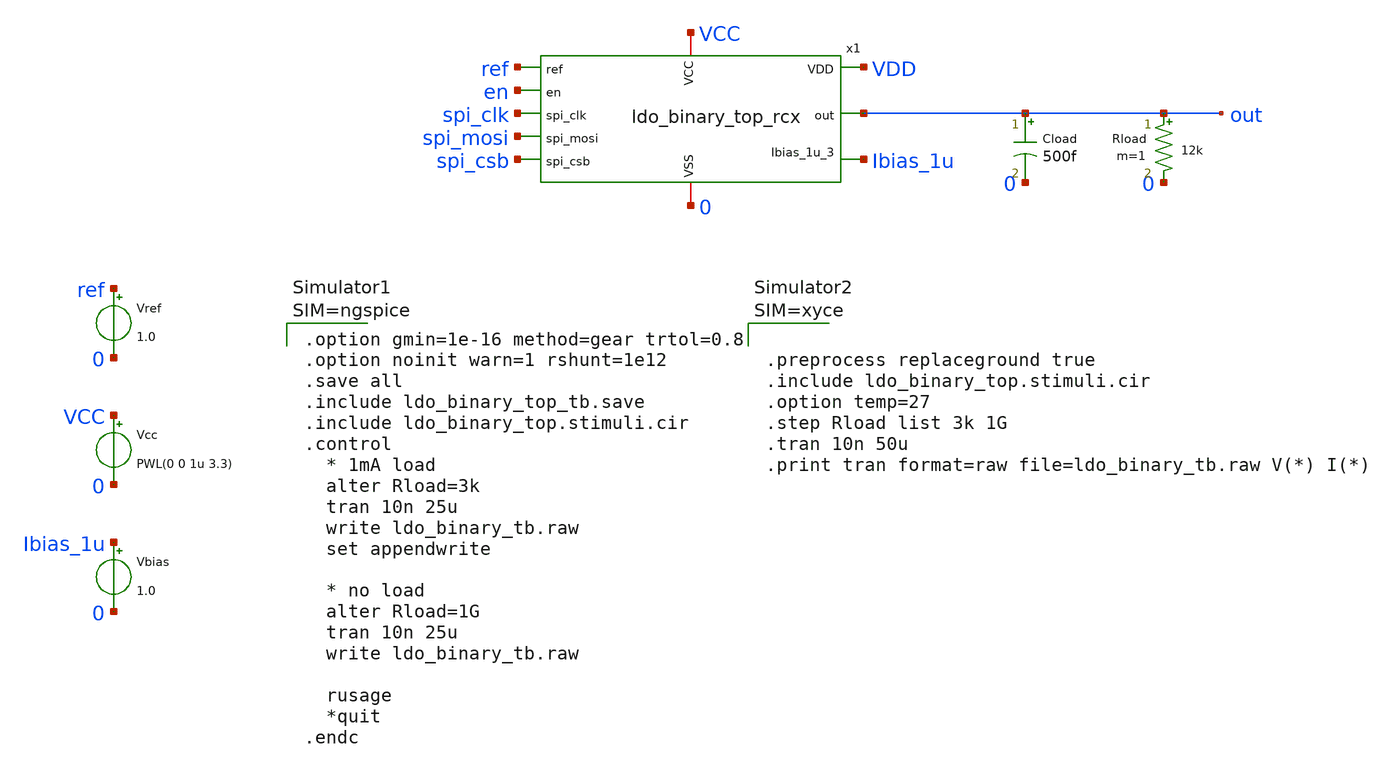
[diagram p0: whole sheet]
** sch_path: FLDO/design_data/xschem/ldo_binary_top_tb_rcx.sch
**.subckt ldo_binary_top_tb_rcx
x1 VCC 0 spi_clk spi_mosi spi_csb ref en out Ibias_1u VDD ldo_binary_top_rcx
Vcc VCC 0 PWL(0 0 1u 3.3)
Vref ref 0 1.0
Cload out 0 500f m=1
Rload out 0 12k m=1
Vbias Ibias_1u 0 1.0
**** begin user architecture code









** IHP models
.lib cornerMOSlv.lib mos_tt
.lib cornerMOShv.lib mos_tt
.lib cornerHBT.lib hbt_typ
.lib cornerRES.lib res_typ
.lib cornerCAP.lib cap_typ

.include sg13g2_stdcell.spice






.option gmin=1e-16 method=gear trtol=0.8
.option noinit warn=1 rshunt=1e12
.save all
.include ldo_binary_top_tb.save
.include ldo_binary_top.stimuli.cir
.control
  * 1mA load
  alter Rload=3k
  tran 10n 25u
  write ldo_binary_tb.raw
  set appendwrite

  * no load
  alter Rload=1G
  tran 10n 25u
  write ldo_binary_tb.raw

  rusage
  *quit
.endc



**** end user architecture code
**.ends

* expanding   symbol:  ldo_binary_top_rcx.sym # of pins=10
** sym_path: FLDO/design_data/xschem/ldo_binary_top.sym
.include [abs_sym_path ../netlist/rcx/ldo_binary_top_rcx.spice]
.end
